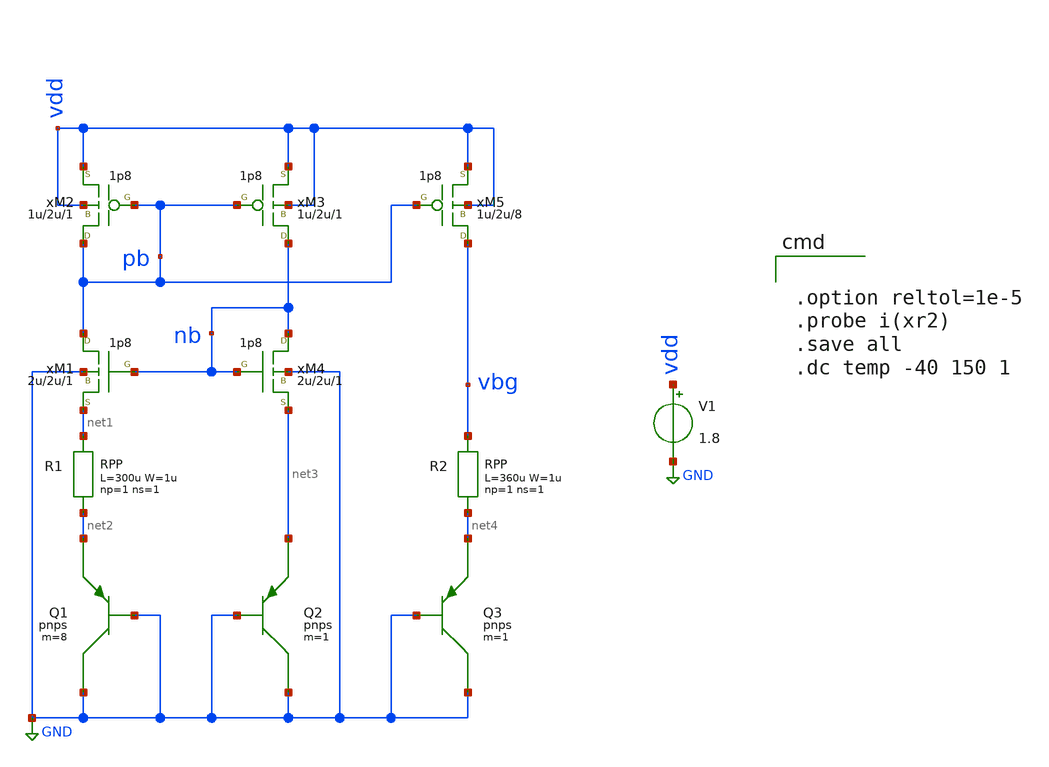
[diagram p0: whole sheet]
** sch_path: xschem/gen18_examples/bg.sch
**.subckt bg
V1 vdd GND 1.8
xR2 vbg net4 RPP W=1u L=360u np=1 ns=1
xR1 net1 net2 RPP W=1u L=300u np=1 ns=1
xM1 pb nb net1 GND nmos18 w=2u l=2u m=1
xM4 nb nb net3 GND nmos18 w=2u l=2u m=1
M2 pb pb vdd vdd pmos18 w=1u l=2u m=1 ad='2*1u *0.18u' as='2*1u *0.18u' pd='2*(1u +2*0.18u)' ps='2*(1u +2*0.18u)'
M3 nb pb vdd vdd pmos18 w=1u l=2u m=1 ad='2*1u *0.18u' as='2*1u *0.18u' pd='2*(1u +2*0.18u)' ps='2*(1u +2*0.18u)'
M5 vbg pb vdd vdd pmos18 w=1u l=2u m=8 ad='2*1u *0.18u' as='2*1u *0.18u' pd='2*(1u +2*0.18u)' ps='2*(1u +2*0.18u)'
Q1 GND GND net2 pnps m=8
Q2 GND GND net3 pnps m=1
Q3 GND GND net4 pnps m=1
**** begin user architecture code

.option reltol=1e-5
.probe i(xr2)
.save all
.dc temp -40 150 1

.include  [path_head [abs_sym_path gen18/gen18models.sym] 3]/mdl/gen18.inc
**** end user architecture code
**.ends
.GLOBAL GND
.end
